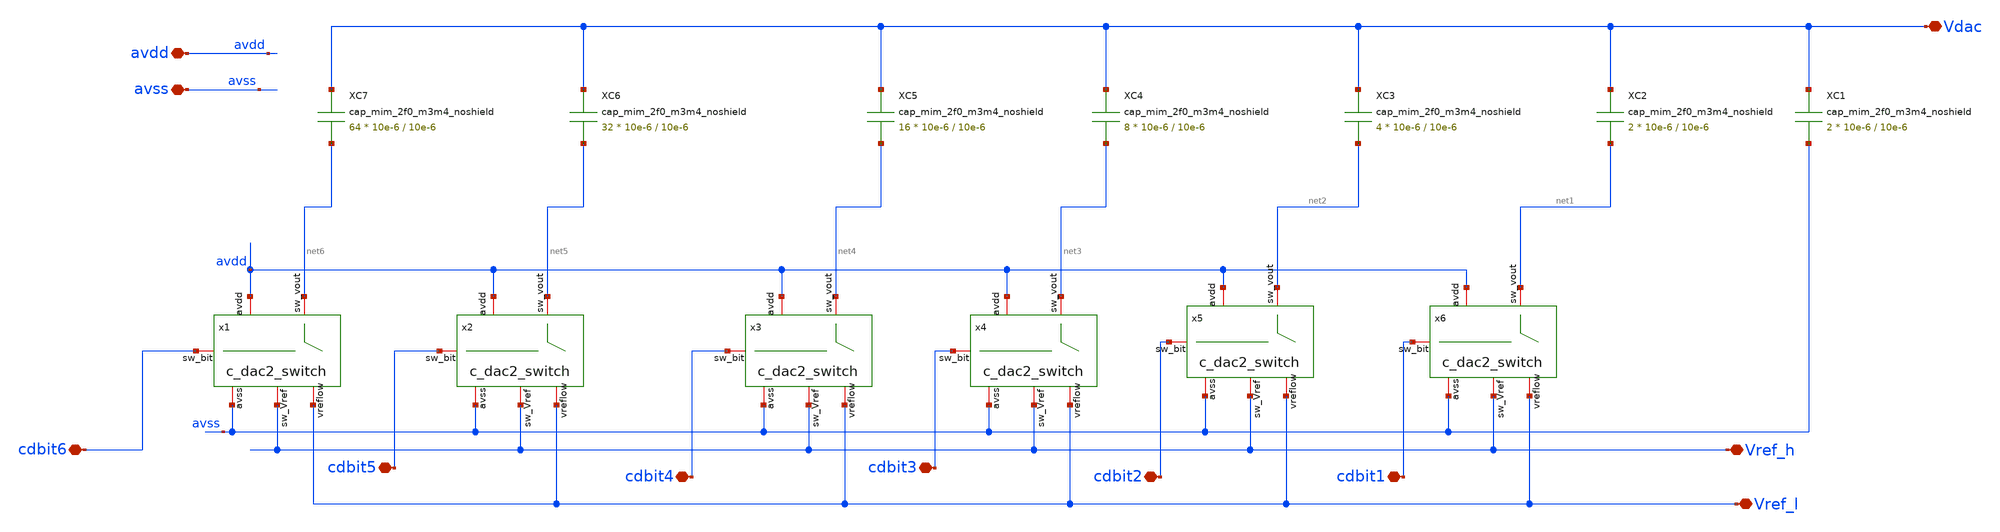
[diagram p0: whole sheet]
** sch_path: designs/libs/WK_Kadam/6bit_CDAC_V2_CO_MK.sch
**.subckt 6bit_CDAC_V2_CO_MK Vref_h Vdac avdd avss cdbit6 cdbit5 cdbit4 cdbit3 cdbit2 cdbit1 Vref_l
*.iopin Vref_h
*.iopin Vdac
*.iopin avdd
*.iopin avss
*.iopin cdbit6
*.iopin cdbit5
*.iopin cdbit4
*.iopin cdbit3
*.iopin cdbit2
*.iopin cdbit1
*.iopin Vref_l
XC3 Vdac net2 cap_mim_2f0_m3m4_noshield c_width=10e-6 c_length=10e-6 m=4
XC4 Vdac net3 cap_mim_2f0_m3m4_noshield c_width=10e-6 c_length=10e-6 m=8
XC5 Vdac net4 cap_mim_2f0_m3m4_noshield c_width=10e-6 c_length=10e-6 m=16
XC6 Vdac net5 cap_mim_2f0_m3m4_noshield c_width=10e-6 c_length=10e-6 m=32
XC7 Vdac net6 cap_mim_2f0_m3m4_noshield c_width=10e-6 c_length=10e-6 m=64
XC1 Vdac avss cap_mim_2f0_m3m4_noshield c_width=10e-6 c_length=10e-6 m=2
XC2 Vdac net1 cap_mim_2f0_m3m4_noshield c_width=10e-6 c_length=10e-6 m=2
x1 net6 cdbit6 avss avdd Vref_h Vref_l c_dac2_switch
x2 net5 cdbit5 avss avdd Vref_h Vref_l c_dac2_switch
x3 net4 cdbit4 avss avdd Vref_h Vref_l c_dac2_switch
x4 net3 cdbit3 avss avdd Vref_h Vref_l c_dac2_switch
x5 net2 cdbit2 avss avdd Vref_h Vref_l c_dac2_switch
x6 net1 cdbit1 avss avdd Vref_h Vref_l c_dac2_switch
**.ends
.end
